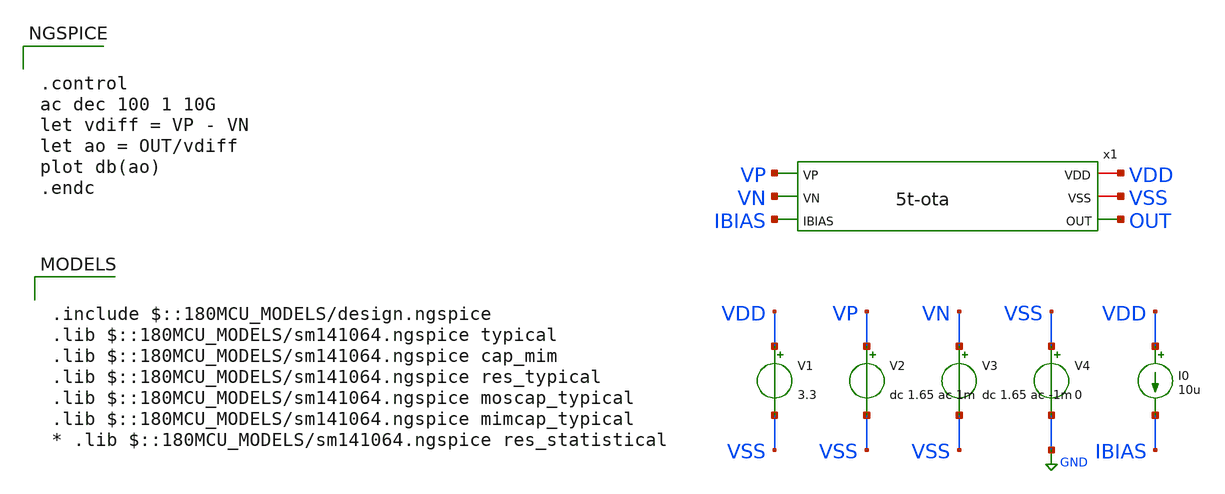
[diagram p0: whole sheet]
** sch_path: w1_advanced-foundation/w1_task/w1_tb/5t-ota-tb.sch
**.subckt 5t-ota-tb
x1 VDD VSS VP VN IBIAS OUT 5t-ota
V1 VDD VSS 3.3
V2 VP VSS dc 1.65 ac 1m
V3 VN VSS dc 1.65 ac -1m
V4 VSS GND 0
I0 VDD IBIAS 10u
**** begin user architecture code

.include $::180MCU_MODELS/design.ngspice
.lib $::180MCU_MODELS/sm141064.ngspice typical
.lib $::180MCU_MODELS/sm141064.ngspice cap_mim
.lib $::180MCU_MODELS/sm141064.ngspice res_typical
.lib $::180MCU_MODELS/sm141064.ngspice moscap_typical
.lib $::180MCU_MODELS/sm141064.ngspice mimcap_typical
* .lib $::180MCU_MODELS/sm141064.ngspice res_statistical



.control
ac dec 100 1 10G
let vdiff = VP - VN
let ao = OUT/vdiff
plot db(ao)
.endc


**** end user architecture code
**.ends

* expanding   symbol:  5t-ota.sym # of pins=6
** sym_path: w1_advanced-foundation/w1_task/w1_tb/5t-ota.sym
** sch_path: w1_advanced-foundation/w1_task/w1_tb/5t-ota.sch
.subckt 5t-ota VDD VSS VP VN IBIAS OUT
*.iopin VDD
*.iopin VSS
*.ipin VP
*.ipin VN
*.ipin IBIAS
*.opin OUT
XM1 OUT VN net1 VSS nfet_03v3 L=2u W=83.875u nf=1 ad='int((nf+1)/2) * W/nf * 0.18u' as='int((nf+2)/2) * W/nf * 0.18u'
+ pd='2*int((nf+1)/2) * (W/nf + 0.18u)' ps='2*int((nf+2)/2) * (W/nf + 0.18u)' nrd='0.18u / W' nrs='0.18u / W'
+ sa=0 sb=0 sd=0 m=4
XM2 net2 VP net1 VSS nfet_03v3 L=2u W=83.875u nf=1 ad='int((nf+1)/2) * W/nf * 0.18u' as='int((nf+2)/2) * W/nf * 0.18u'
+ pd='2*int((nf+1)/2) * (W/nf + 0.18u)' ps='2*int((nf+2)/2) * (W/nf + 0.18u)' nrd='0.18u / W' nrs='0.18u / W'
+ sa=0 sb=0 sd=0 m=4
XM3 net2 net2 VDD VDD pfet_03v3 L=2u W=55u nf=1 ad='int((nf+1)/2) * W/nf * 0.18u' as='int((nf+2)/2) * W/nf * 0.18u'
+ pd='2*int((nf+1)/2) * (W/nf + 0.18u)' ps='2*int((nf+2)/2) * (W/nf + 0.18u)' nrd='0.18u / W' nrs='0.18u / W'
+ sa=0 sb=0 sd=0 m=32
XM4 OUT net2 VDD VDD pfet_03v3 L=2u W=55u nf=1 ad='int((nf+1)/2) * W/nf * 0.18u' as='int((nf+2)/2) * W/nf * 0.18u'
+ pd='2*int((nf+1)/2) * (W/nf + 0.18u)' ps='2*int((nf+2)/2) * (W/nf + 0.18u)' nrd='0.18u / W' nrs='0.18u / W'
+ sa=0 sb=0 sd=0 m=1
XM5 net1 IBIAS VSS VSS nfet_03v3 L=2u W=67.67u nf=1 ad='int((nf+1)/2) * W/nf * 0.18u' as='int((nf+2)/2) * W/nf * 0.18u'
+ pd='2*int((nf+1)/2) * (W/nf + 0.18u)' ps='2*int((nf+2)/2) * (W/nf + 0.18u)' nrd='0.18u / W' nrs='0.18u / W'
+ sa=0 sb=0 sd=0 m=32
XM6 IBIAS IBIAS VSS VSS nfet_03v3 L=2u W=40u nf=1 ad='int((nf+1)/2) * W/nf * 0.18u' as='int((nf+2)/2) * W/nf * 0.18u'
+ pd='2*int((nf+1)/2) * (W/nf + 0.18u)' ps='2*int((nf+2)/2) * (W/nf + 0.18u)' nrd='0.18u / W' nrs='0.18u / W'
+ sa=0 sb=0 sd=0 m=1
.ends

.GLOBAL GND
.end
